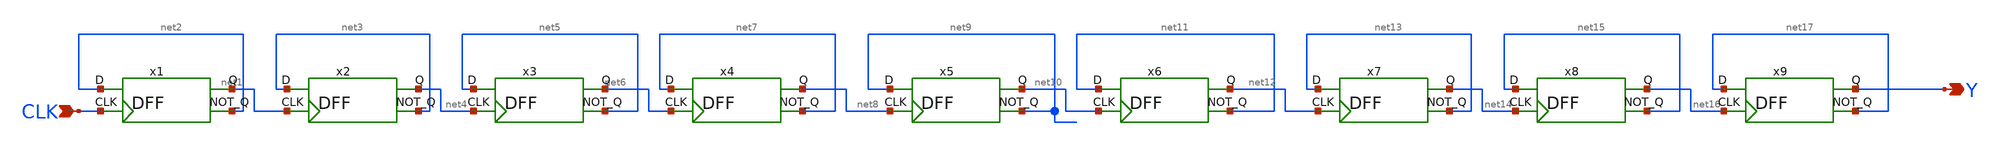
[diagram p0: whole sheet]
** sch_path: library/xschem/9bit_count.sch
**.subckt 9bit_count CLK Y
*.ipin CLK
*.opin Y
x1 net1 net2 CLK net2 DFF
x2 net4 net3 net1 net3 DFF
x3 net6 net5 net4 net5 DFF
x4 net8 net7 net6 net7 DFF
x5 net10 net9 net8 net9 DFF
x6 net12 net11 net10 net11 DFF
x7 net14 net13 net12 net13 DFF
x8 net16 net15 net14 net15 DFF
x9 Y net17 net16 net17 DFF
**.ends

* expanding   symbol:  DFF.sym # of pins=4
** sym_path: library/xschem/DFF.sym
** sch_path: library/xschem/DFF.sch
.subckt DFF Q D CLK NOT_Q
*.ipin D
*.opin Q
*.opin NOT_Q
*.ipin CLK
x1 net2 net1 Q NOT_Q Dlatch
x2 D CLK net2 net3 Dlatch
x3 CLK net1 inv
.ends


* expanding   symbol:  Dlatch.sym # of pins=4
** sym_path: library/xschem/Dlatch.sym
** sch_path: library/xschem/Dlatch.sch
.subckt Dlatch D CLK Q NOT_Q
*.ipin D
*.ipin CLK
*.opin Q
*.opin NOT_Q
XM1 net1 CLK net2 GND sky130_fd_pr__nfet_01v8 L=0.15 W=1 nf=1 ad='int((nf+1)/2) * W/nf * 0.29' as='int((nf+2)/2) * W/nf * 0.29'
+ pd='2*int((nf+1)/2) * (W/nf + 0.29)' ps='2*int((nf+2)/2) * (W/nf + 0.29)' nrd='0.29 / W' nrs='0.29 / W'
+ sa=0 sb=0 sd=0 mult=1 m=1
XM2 net1 D VDD VDD sky130_fd_pr__pfet_01v8 L=0.15 W=1 nf=1 ad='int((nf+1)/2) * W/nf * 0.29' as='int((nf+2)/2) * W/nf * 0.29'
+ pd='2*int((nf+1)/2) * (W/nf + 0.29)' ps='2*int((nf+2)/2) * (W/nf + 0.29)' nrd='0.29 / W' nrs='0.29 / W'
+ sa=0 sb=0 sd=0 mult=1 m=1
XM3 net1 CLK VDD VDD sky130_fd_pr__pfet_01v8 L=0.15 W=1 nf=1 ad='int((nf+1)/2) * W/nf * 0.29' as='int((nf+2)/2) * W/nf * 0.29'
+ pd='2*int((nf+1)/2) * (W/nf + 0.29)' ps='2*int((nf+2)/2) * (W/nf + 0.29)' nrd='0.29 / W' nrs='0.29 / W'
+ sa=0 sb=0 sd=0 mult=1 m=1
XM4 net2 D GND GND sky130_fd_pr__nfet_01v8 L=0.15 W=1 nf=1 ad='int((nf+1)/2) * W/nf * 0.29' as='int((nf+2)/2) * W/nf * 0.29'
+ pd='2*int((nf+1)/2) * (W/nf + 0.29)' ps='2*int((nf+2)/2) * (W/nf + 0.29)' nrd='0.29 / W' nrs='0.29 / W'
+ sa=0 sb=0 sd=0 mult=1 m=1
XM5 Q NOT_Q net3 GND sky130_fd_pr__nfet_01v8 L=0.15 W=1 nf=1 ad='int((nf+1)/2) * W/nf * 0.29' as='int((nf+2)/2) * W/nf * 0.29'
+ pd='2*int((nf+1)/2) * (W/nf + 0.29)' ps='2*int((nf+2)/2) * (W/nf + 0.29)' nrd='0.29 / W' nrs='0.29 / W'
+ sa=0 sb=0 sd=0 mult=1 m=1
XM6 Q net1 VDD VDD sky130_fd_pr__pfet_01v8 L=0.15 W=1 nf=1 ad='int((nf+1)/2) * W/nf * 0.29' as='int((nf+2)/2) * W/nf * 0.29'
+ pd='2*int((nf+1)/2) * (W/nf + 0.29)' ps='2*int((nf+2)/2) * (W/nf + 0.29)' nrd='0.29 / W' nrs='0.29 / W'
+ sa=0 sb=0 sd=0 mult=1 m=1
XM7 Q NOT_Q VDD VDD sky130_fd_pr__pfet_01v8 L=0.15 W=1 nf=1 ad='int((nf+1)/2) * W/nf * 0.29' as='int((nf+2)/2) * W/nf * 0.29'
+ pd='2*int((nf+1)/2) * (W/nf + 0.29)' ps='2*int((nf+2)/2) * (W/nf + 0.29)' nrd='0.29 / W' nrs='0.29 / W'
+ sa=0 sb=0 sd=0 mult=1 m=1
XM8 net3 net1 GND GND sky130_fd_pr__nfet_01v8 L=0.15 W=1 nf=1 ad='int((nf+1)/2) * W/nf * 0.29' as='int((nf+2)/2) * W/nf * 0.29'
+ pd='2*int((nf+1)/2) * (W/nf + 0.29)' ps='2*int((nf+2)/2) * (W/nf + 0.29)' nrd='0.29 / W' nrs='0.29 / W'
+ sa=0 sb=0 sd=0 mult=1 m=1
XM9 NOT_Q net5 net4 GND sky130_fd_pr__nfet_01v8 L=0.15 W=1 nf=1 ad='int((nf+1)/2) * W/nf * 0.29' as='int((nf+2)/2) * W/nf * 0.29'
+ pd='2*int((nf+1)/2) * (W/nf + 0.29)' ps='2*int((nf+2)/2) * (W/nf + 0.29)' nrd='0.29 / W' nrs='0.29 / W'
+ sa=0 sb=0 sd=0 mult=1 m=1
XM10 NOT_Q Q VDD VDD sky130_fd_pr__pfet_01v8 L=0.15 W=1 nf=1 ad='int((nf+1)/2) * W/nf * 0.29' as='int((nf+2)/2) * W/nf * 0.29'
+ pd='2*int((nf+1)/2) * (W/nf + 0.29)' ps='2*int((nf+2)/2) * (W/nf + 0.29)' nrd='0.29 / W' nrs='0.29 / W'
+ sa=0 sb=0 sd=0 mult=1 m=1
XM11 NOT_Q net5 VDD VDD sky130_fd_pr__pfet_01v8 L=0.15 W=1 nf=1 ad='int((nf+1)/2) * W/nf * 0.29' as='int((nf+2)/2) * W/nf * 0.29'
+ pd='2*int((nf+1)/2) * (W/nf + 0.29)' ps='2*int((nf+2)/2) * (W/nf + 0.29)' nrd='0.29 / W' nrs='0.29 / W'
+ sa=0 sb=0 sd=0 mult=1 m=1
XM12 net4 Q GND GND sky130_fd_pr__nfet_01v8 L=0.15 W=1 nf=1 ad='int((nf+1)/2) * W/nf * 0.29' as='int((nf+2)/2) * W/nf * 0.29'
+ pd='2*int((nf+1)/2) * (W/nf + 0.29)' ps='2*int((nf+2)/2) * (W/nf + 0.29)' nrd='0.29 / W' nrs='0.29 / W'
+ sa=0 sb=0 sd=0 mult=1 m=1
XM13 net5 net7 net6 GND sky130_fd_pr__nfet_01v8 L=0.15 W=1 nf=1 ad='int((nf+1)/2) * W/nf * 0.29' as='int((nf+2)/2) * W/nf * 0.29'
+ pd='2*int((nf+1)/2) * (W/nf + 0.29)' ps='2*int((nf+2)/2) * (W/nf + 0.29)' nrd='0.29 / W' nrs='0.29 / W'
+ sa=0 sb=0 sd=0 mult=1 m=1
XM14 net5 CLK VDD VDD sky130_fd_pr__pfet_01v8 L=0.15 W=1 nf=1 ad='int((nf+1)/2) * W/nf * 0.29' as='int((nf+2)/2) * W/nf * 0.29'
+ pd='2*int((nf+1)/2) * (W/nf + 0.29)' ps='2*int((nf+2)/2) * (W/nf + 0.29)' nrd='0.29 / W' nrs='0.29 / W'
+ sa=0 sb=0 sd=0 mult=1 m=1
XM15 net5 net7 VDD VDD sky130_fd_pr__pfet_01v8 L=0.15 W=1 nf=1 ad='int((nf+1)/2) * W/nf * 0.29' as='int((nf+2)/2) * W/nf * 0.29'
+ pd='2*int((nf+1)/2) * (W/nf + 0.29)' ps='2*int((nf+2)/2) * (W/nf + 0.29)' nrd='0.29 / W' nrs='0.29 / W'
+ sa=0 sb=0 sd=0 mult=1 m=1
XM16 net6 CLK GND GND sky130_fd_pr__nfet_01v8 L=0.15 W=1 nf=1 ad='int((nf+1)/2) * W/nf * 0.29' as='int((nf+2)/2) * W/nf * 0.29'
+ pd='2*int((nf+1)/2) * (W/nf + 0.29)' ps='2*int((nf+2)/2) * (W/nf + 0.29)' nrd='0.29 / W' nrs='0.29 / W'
+ sa=0 sb=0 sd=0 mult=1 m=1
XM17 net7 D GND GND sky130_fd_pr__nfet_01v8 L=0.15 W=1 nf=1 ad='int((nf+1)/2) * W/nf * 0.29' as='int((nf+2)/2) * W/nf * 0.29'
+ pd='2*int((nf+1)/2) * (W/nf + 0.29)' ps='2*int((nf+2)/2) * (W/nf + 0.29)' nrd='0.29 / W' nrs='0.29 / W'
+ sa=0 sb=0 sd=0 mult=1 m=1
XM18 net7 D VDD VDD sky130_fd_pr__pfet_01v8 L=0.15 W=1 nf=1 ad='int((nf+1)/2) * W/nf * 0.29' as='int((nf+2)/2) * W/nf * 0.29'
+ pd='2*int((nf+1)/2) * (W/nf + 0.29)' ps='2*int((nf+2)/2) * (W/nf + 0.29)' nrd='0.29 / W' nrs='0.29 / W'
+ sa=0 sb=0 sd=0 mult=1 m=1
.ends


* expanding   symbol:  inv.sym # of pins=2
** sym_path: library/xschem/inv.sym
** sch_path: library/xschem/inv.sch
.subckt inv A Y
*.opin Y
*.ipin A
XM1 Y A GND GND sky130_fd_pr__nfet_01v8 L=0.15 W=1 nf=1 ad='int((nf+1)/2) * W/nf * 0.29' as='int((nf+2)/2) * W/nf * 0.29'
+ pd='2*int((nf+1)/2) * (W/nf + 0.29)' ps='2*int((nf+2)/2) * (W/nf + 0.29)' nrd='0.29 / W' nrs='0.29 / W'
+ sa=0 sb=0 sd=0 mult=1 m=1
XM2 Y A VDD VDD sky130_fd_pr__pfet_01v8 L=0.15 W=1 nf=1 ad='int((nf+1)/2) * W/nf * 0.29' as='int((nf+2)/2) * W/nf * 0.29'
+ pd='2*int((nf+1)/2) * (W/nf + 0.29)' ps='2*int((nf+2)/2) * (W/nf + 0.29)' nrd='0.29 / W' nrs='0.29 / W'
+ sa=0 sb=0 sd=0 mult=1 m=1
.ends

.GLOBAL VDD
.GLOBAL GND
.end
